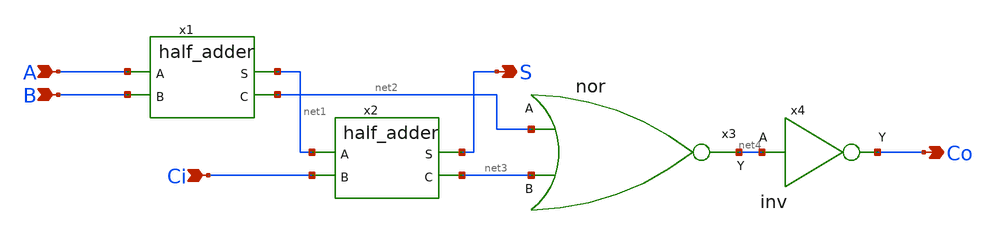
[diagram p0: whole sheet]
** sch_path: circuits/xschem/full_adder.sch
**.subckt full_adder A B Ci S Co
*.ipin A
*.ipin B
*.ipin Ci
*.opin S
*.opin Co
x1 A net1 B net2 half_adder
x2 net1 S Ci net3 half_adder
x3 net4 net2 net3 nor
x4 Co net4 inv
**.ends
.end
